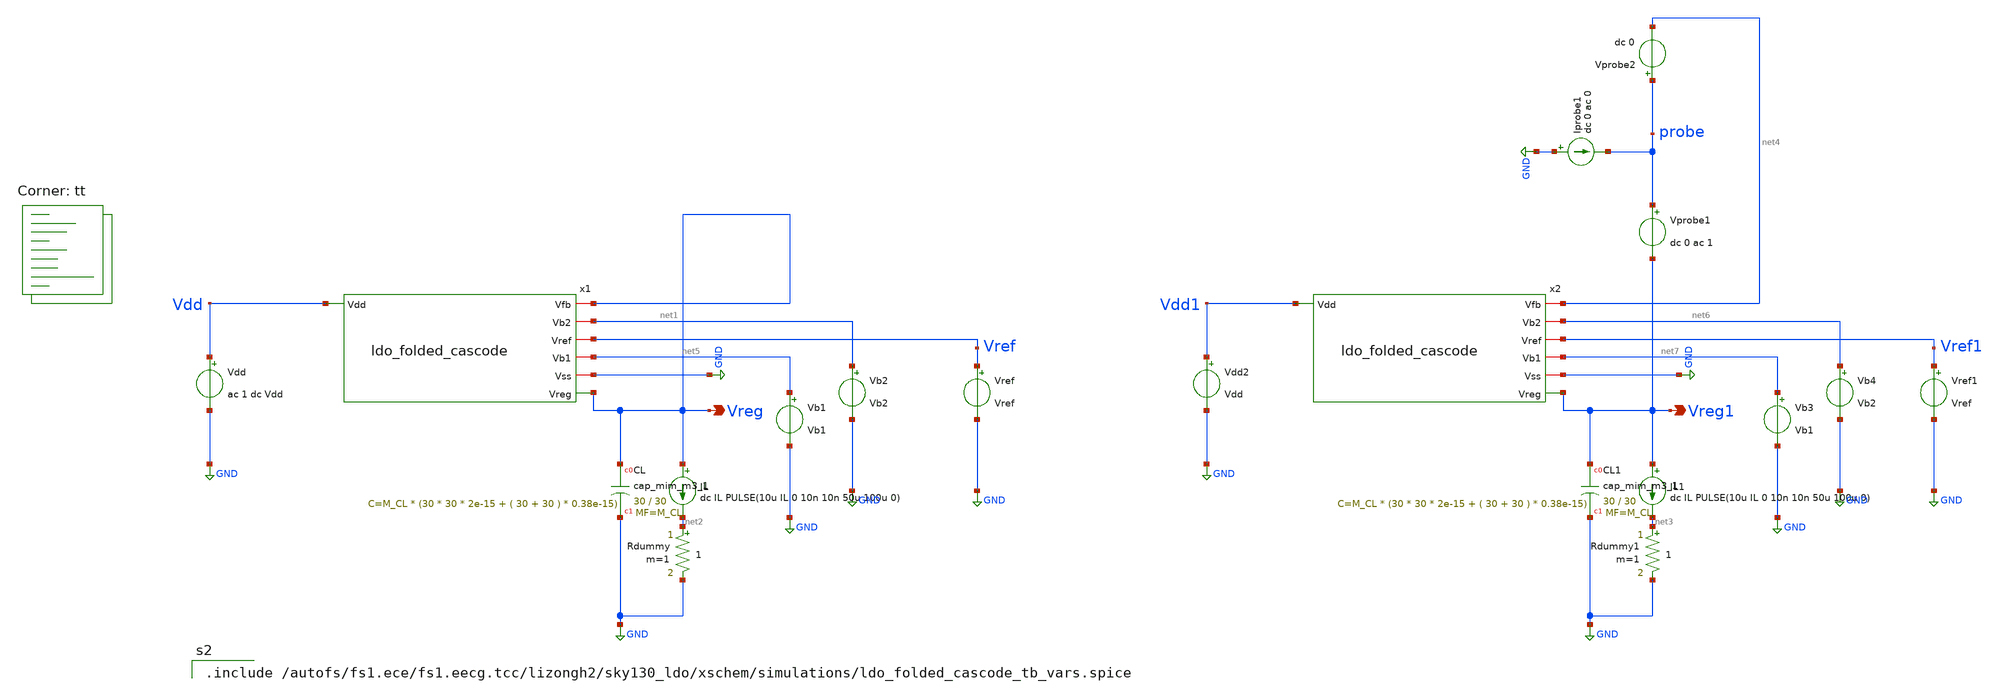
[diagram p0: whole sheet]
** sch_path: xschem/ldo_folded_cascode_tb.sch
**.subckt ldo_folded_cascode_tb Vreg Vreg1
*.opin Vreg
*.opin Vreg1
Vref Vref GND Vref
IL Vreg net2 dc IL PULSE(10u IL 0 10n 10n 50u 100u 0)
Vdd Vdd GND ac 1 dc Vdd
XCL Vreg GND sky130_fd_pr__cap_mim_m3_1 W=30 L=30 MF=M_CL m=M_CL
Rdummy net2 GND 1 m=1
x1 Vdd Vreg net1 Vref net5 GND Vreg ldo_folded_cascode
Vref1 Vref1 GND Vref
IL1 Vreg1 net3 dc IL PULSE(10u IL 0 10n 10n 50u 100u 0)
Vdd2 Vdd1 GND Vdd
XCL1 Vreg1 GND sky130_fd_pr__cap_mim_m3_1 W=30 L=30 MF=M_CL m=M_CL
Rdummy1 net3 GND 1 m=1
x2 Vdd1 net4 net6 Vref1 net7 GND Vreg1 ldo_folded_cascode
Vprobe2 probe net4 dc 0
Vprobe1 probe Vreg1 dc 0 ac 1
Iprobe1 GND probe dc 0 ac 0
Vb2 net1 GND Vb2
Vb1 net5 GND Vb1
Vb4 net6 GND Vb2
Vb3 net7 GND Vb1
**** begin user architecture code

.include /autofs/fs1.ece/fs1.eecg.tcc/lizongh2/sky130_ldo/xschem/simulations/ldo_folded_cascode_tb_vars.spice




.nodeset v(Vreg)=1.8
.nodeset v(Vreg1)=1.8

.control
* high precision simulation
*.OPTIONS maxord=1
.OPTIONS itl1=200
.OPTIONS itl2=200
.OPTIONS itl4=200

* save all voltage and current
save all
.options savecurrents
set filetype=ascii
set units=degrees

* Loop stability
alter IL1 dc=10u
let runs=2
let run=0

alter @Vprobe1[acmag]=1
alter @Iprobe1[acmag]=0

dowhile run<runs
set run=$&run
set temp=27

ac dec 10 1 10G

alter @Vprobe1[acmag]=0
alter @Iprobe1[acmag]=1

let run=run+1
end

let ip11 = ac1.i(Vprobe1)
let ip12 = ac1.i(Vprobe2)
let ip21 = ac2.i(Vprobe1)
let ip22 = ac2.i(Vprobe2)
let vprb1 = ac1.v(probe)
let vprb2 = ac2.v(probe)

*** Middlebrook
let mb = 1/(vprb1+ip22)-1
*** Tian that is preferred
let av = 1/(1/(2*(ip11*vprb2-vprb1*ip21)+vprb1+ip21)-1)

plot vdb(mb) vp(mb)
plot vdb(av) vp(av)

wrdata ldo_folded_cascode_tb_loop_gain_minload mag(av) vp(av)

* at max load
reset all
alter IL1 dc=10m
let runs=2
let run=0

alter @Vprobe1[acmag]=1
alter @Iprobe1[acmag]=0

dowhile run<runs
set run=$&run
set temp=27

ac dec 10 1 10G

alter @Vprobe1[acmag]=0
alter @Iprobe1[acmag]=1

let run=run+1
end

let ip11 = ac3.i(Vprobe1)
let ip12 = ac3.i(Vprobe2)
let ip21 = ac4.i(Vprobe1)
let ip22 = ac4.i(Vprobe2)
let vprb1 = ac3.v(probe)
let vprb2 = ac4.v(probe)

*** Middlebrook
let mb = 1/(vprb1+ip22)-1
*** Tian that is preferred
let av = 1/(1/(2*(ip11*vprb2-vprb1*ip21)+vprb1+ip21)-1)

plot vdb(mb) vp(mb)
plot vdb(av) vp(av)

wrdata ldo_folded_cascode_tb_loop_gain_maxload mag(av) vp(av)

* DC sweep
dc Vdd 1 3 0.01
plot v(Vdd) v(Vreg)
wrdata ldo_folded_cascode_tb_dc v(Vreg)

* Transient analysis with load regulation
* do not miss the space between the square bracket and number
tran 10n 100u
plot @Rdummy[i]
plot Vreg
wrdata ldo_folded_cascode_tb_load_reg Vreg

* Transient analysis with line regulation
* at minimum load current 10uA
*alter @IL[PULSE] [ 10u 10u 0 10n 10n 100u 100u 0 ]
*alter @Vdd[PULSE] [ 2 2.5 0 1u 1u 25u 50u 0 ]
*tran 10n 100u
*plot Vdd
*plot @Rdummy[i]
*plot Vreg
*wrdata ldo_folded_cascode_tb_line_reg_minload Vreg

* at maximum load current 10mA
*alter @IL[PULSE] [ 10m 10m 0 10n 10n 100u 100u 0 ]
*tran 10n 100u
*plot @Rdummy[i]
*plot Vreg
*wrdata ldo_folded_cascode_tb_line_reg_maxload Vreg


* PSRR with max load
alter Vdd ac=1
alter Vprobe1 ac=0
ac dec 10 1 10G
plot vdb(Vreg)
wrdata ldo_folded_cascode_tb_psrr_maxload mag(Vreg) vp(Vreg)

* PSRR with min load
alter IL dc=10u
ac dec 10 1 10G
plot vdb(Vreg)
wrdata ldo_folded_cascode_tb_psrr_minload mag(Vreg) vp(Vreg)
*min load do a pz analysis
pz Vdd GND Vreg GND vol pz
print pole(1) pole(2) pole(3) pole(4) pole(5) pole(6) pole(7) pole(8) pole(9)
print zero(1) zero(2) zero(3) zero(4) zero(5) zero(6) zero(7) zero(8) zero(9)

* OP
op
alter IL dc=10u
.include /autofs/fs1.ece/fs1.eecg.tcc/lizongh2/sky130_ldo/python/ldo/simulations/ldo_folded_cascode_tb_dev_params.spice
.endc


.lib $::SKYWATER_MODELS/sky130.lib.spice tt
**** end user architecture code
**.ends

* expanding   symbol:  ldo_folded_cascode.sym # of pins=7
** sym_path: xschem/ldo_folded_cascode.sym
** sch_path: xschem/ldo_folded_cascode.sch
.subckt ldo_folded_cascode Vdd Vfb Vb2 Vref Vb1 Vss Vreg
*.iopin Vss
*.opin Vreg
*.iopin Vref
*.ipin Vdd
*.iopin Vfb
*.iopin Vb2
*.iopin Vb1
XM10 Vreg net1 Vdd Vdd sky130_fd_pr__pfet_g5v0d10v5 L=L_pass W=W_pass nf=1 ad='int((nf+1)/2) * W/nf * 0.29'
+ as='int((nf+2)/2) * W/nf * 0.29' pd='2*int((nf+1)/2) * (W/nf + 0.29)' ps='2*int((nf+2)/2) * (W/nf + 0.29)'
+ nrd='0.29 / W' nrs='0.29 / W' sa=0 sb=0 sd=0 mult=M_pass m=M_pass
x1 Vdd Vb2 Vfb Vref net1 Vb1 Vss diff_pair_folded_cascode
XCfb net2 Vreg sky130_fd_pr__cap_mim_m3_1 W=10 L=10 MF=M_Cfb m=M_Cfb
XRfb net2 net1 Vss sky130_fd_pr__res_high_po_0p35 L=3 mult=M_Rfb m=M_Rfb
.ends


* expanding   symbol:  diff_pair_folded_cascode.sym # of pins=7
** sym_path: xschem/diff_pair_folded_cascode.sym
** sch_path: xschem/diff_pair_folded_cascode.sch
.subckt diff_pair_folded_cascode Vdd Vb2 vinp vinm vout Vb1 Vss
*.iopin Vdd
*.ipin vinm
*.ipin vinp
*.iopin Vb1
*.iopin Vss
*.iopin Vb2
*.opin vout
XM1 net2 vinp net4 Vss sky130_fd_pr__nfet_g5v0d10v5 L=L_M1 W=W_M1 nf=1 ad='int((nf+1)/2) * W/nf * 0.29'
+ as='int((nf+2)/2) * W/nf * 0.29' pd='2*int((nf+1)/2) * (W/nf + 0.29)' ps='2*int((nf+2)/2) * (W/nf + 0.29)'
+ nrd='0.29 / W' nrs='0.29 / W' sa=0 sb=0 sd=0 mult=1 m=1
XM2 net3 vinm net4 Vss sky130_fd_pr__nfet_g5v0d10v5 L=L_M2 W=W_M2 nf=1 ad='int((nf+1)/2) * W/nf * 0.29'
+ as='int((nf+2)/2) * W/nf * 0.29' pd='2*int((nf+1)/2) * (W/nf + 0.29)' ps='2*int((nf+2)/2) * (W/nf + 0.29)'
+ nrd='0.29 / W' nrs='0.29 / W' sa=0 sb=0 sd=0 mult=1 m=1
XM4 net3 net1 Vdd Vdd sky130_fd_pr__pfet_g5v0d10v5 L=L_M4 W=W_M4 nf=1 ad='int((nf+1)/2) * W/nf * 0.29'
+ as='int((nf+2)/2) * W/nf * 0.29' pd='2*int((nf+1)/2) * (W/nf + 0.29)' ps='2*int((nf+2)/2) * (W/nf + 0.29)'
+ nrd='0.29 / W' nrs='0.29 / W' sa=0 sb=0 sd=0 mult=1 m=1
XM3 net2 net1 Vdd Vdd sky130_fd_pr__pfet_g5v0d10v5 L=L_M3 W=W_M3 nf=1 ad='int((nf+1)/2) * W/nf * 0.29'
+ as='int((nf+2)/2) * W/nf * 0.29' pd='2*int((nf+1)/2) * (W/nf + 0.29)' ps='2*int((nf+2)/2) * (W/nf + 0.29)'
+ nrd='0.29 / W' nrs='0.29 / W' sa=0 sb=0 sd=0 mult=1 m=1
XM9 net4 Vb1 Vss Vss sky130_fd_pr__nfet_g5v0d10v5 L=L_M9 W=W_M9 nf=1 ad='int((nf+1)/2) * W/nf * 0.29'
+ as='int((nf+2)/2) * W/nf * 0.29' pd='2*int((nf+1)/2) * (W/nf + 0.29)' ps='2*int((nf+2)/2) * (W/nf + 0.29)'
+ nrd='0.29 / W' nrs='0.29 / W' sa=0 sb=0 sd=0 mult=1 m=1
XM6 vout Vb2 net3 Vdd sky130_fd_pr__pfet_g5v0d10v5 L=L_M6 W=W_M6 nf=1 ad='int((nf+1)/2) * W/nf * 0.29'
+ as='int((nf+2)/2) * W/nf * 0.29' pd='2*int((nf+1)/2) * (W/nf + 0.29)' ps='2*int((nf+2)/2) * (W/nf + 0.29)'
+ nrd='0.29 / W' nrs='0.29 / W' sa=0 sb=0 sd=0 mult=1 m=1
XM5 net1 Vb2 net2 Vdd sky130_fd_pr__pfet_g5v0d10v5 L=L_M5 W=W_M5 nf=1 ad='int((nf+1)/2) * W/nf * 0.29'
+ as='int((nf+2)/2) * W/nf * 0.29' pd='2*int((nf+1)/2) * (W/nf + 0.29)' ps='2*int((nf+2)/2) * (W/nf + 0.29)'
+ nrd='0.29 / W' nrs='0.29 / W' sa=0 sb=0 sd=0 mult=1 m=1
XM7 net1 Vb1 Vss Vss sky130_fd_pr__nfet_g5v0d10v5 L=L_M7 W=W_M7 nf=1 ad='int((nf+1)/2) * W/nf * 0.29'
+ as='int((nf+2)/2) * W/nf * 0.29' pd='2*int((nf+1)/2) * (W/nf + 0.29)' ps='2*int((nf+2)/2) * (W/nf + 0.29)'
+ nrd='0.29 / W' nrs='0.29 / W' sa=0 sb=0 sd=0 mult=1 m=1
XM8 vout Vb1 Vss Vss sky130_fd_pr__nfet_g5v0d10v5 L=L_M8 W=W_M8 nf=1 ad='int((nf+1)/2) * W/nf * 0.29'
+ as='int((nf+2)/2) * W/nf * 0.29' pd='2*int((nf+1)/2) * (W/nf + 0.29)' ps='2*int((nf+2)/2) * (W/nf + 0.29)'
+ nrd='0.29 / W' nrs='0.29 / W' sa=0 sb=0 sd=0 mult=1 m=1
.ends

.GLOBAL GND
.end
